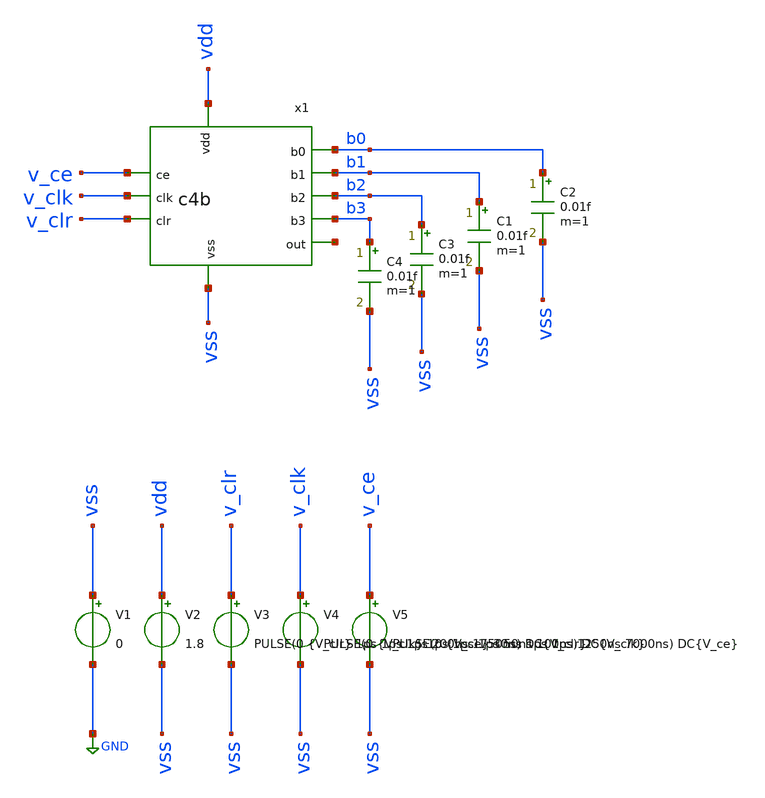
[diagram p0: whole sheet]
** sch_path: track_vlsi/martinez-sapriza/sch/tb_c4b.sch
**.subckt tb_c4b
V1 vss GND 0
V2 vdd vss 1.8
C1 b1 vss 0.01f m=1
V3 v_clr vss PULSE(0 {V_clr} 1ps 1ps 1ps 200ns 1750ns) DC{V_clr}
V4 v_clk vss PULSE(0 {V_clk} 1ps 1ps 1ps 50ns 100ns) DC{V_clk}
V5 v_ce vss PULSE(0 {V_ce} 30ns 1ps 1ps 1250ns 7000ns) DC{V_ce}
C2 b0 vss 0.01f m=1
C3 b2 vss 0.01f m=1
C4 b3 vss 0.01f m=1
x1 v_ce v_clk v_clr vdd vss b0 b1 b2 b3 net1 c4b
**** begin user architecture code



* Circuit parameters
.param V_clk = 1.8
.param V_clr = 1.8
.param V_ce = 1.8
.options TEMP = 27.0

* Include
.lib /home/eamta/skywater/skywater-pdk/libraries/sky130_fd_pr_ngspice/latest/models/corners/sky130.lib TT

* Signals to save
.save all

* Simulation
.control
  tran 10n 2000ns
  setplot tran1
  plot v(v_clr) v(v_clk) v(v_ce)
  write tb_c4b_tran1.raw

  tran 10n 2000ns
  setplot tran2
  plot v(b0)
  write tb_c4b_tran2.raw

 tran 10n 2000ns
  setplot tran3
  plot v(b1)
  write tb_c4b_tran3.raw

 tran 10n 2000ns
  setplot tran4
  plot v(b2)
  write tb_c4b_tran4.raw

 tran 10n 2000ns
  setplot tran5
  plot v(b3)
  write tb_c4b_tran5.raw

.endc

.end



**** end user architecture code
**.ends
.GLOBAL GND
.end
